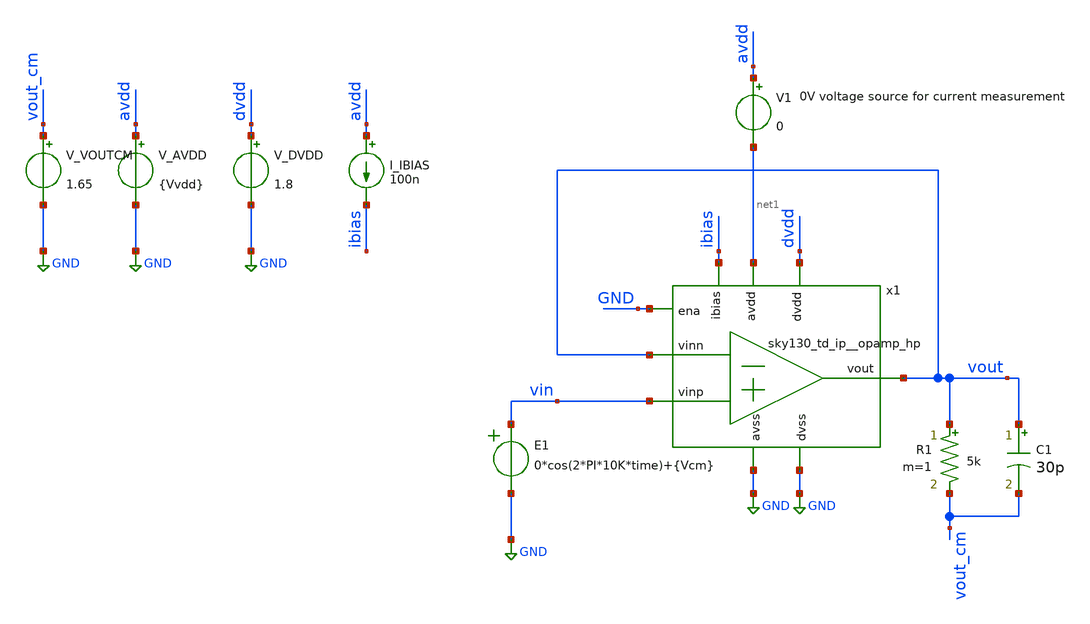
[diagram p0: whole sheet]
** sch_path: cace/ivdd_disabled.sch
**.subckt ivdd_disabled
x1 net1 vout ibias vout vin GND dvdd GND GND sky130_td_ip__opamp_hp
V_AVDD avdd GND {Vvdd}
.save i(v_avdd)
V_DVDD dvdd GND 1.8
.save i(v_dvdd)
I_IBIAS avdd ibias 100n
R1 vout vout_cm 5k m=1
C1 vout vout_cm 30p m=1
V_VOUTCM vout_cm GND 1.65
.save i(v_voutcm)
E1 vin GND VOL=' 0*cos(2*PI*10K*time)+{Vcm} '
V1 avdd net1 0
.save i(v1)
**** begin user architecture code


.control
save all

tran 100n 10u
run

let i_avdd = i(V1)
meas tran max_iavdd MAX i_avdd

echo Max current (disabled): $&max_iavdd

echo $&max_iavdd > {simpath}/{filename}_{N}.data
quit
.endc




* CACE gensim simulation file {filename}_{N}
* Generated by CACE gensim, Efabless Corporation (c) 2023
* Find the power supply rejection ratio of the amplifier

.include {DUT_path}

.lib {PDK_ROOT}/{PDK}/libs.tech/combined/sky130.lib.spice {corner}

.option TEMP={temperature}
* Flag unsafe operating conditions (exceeds models' specified limits)
.option warn=1
.option SEED=[{seed=12345} + {iterations=0}]


**** end user architecture code
**.ends
.GLOBAL GND
.end
